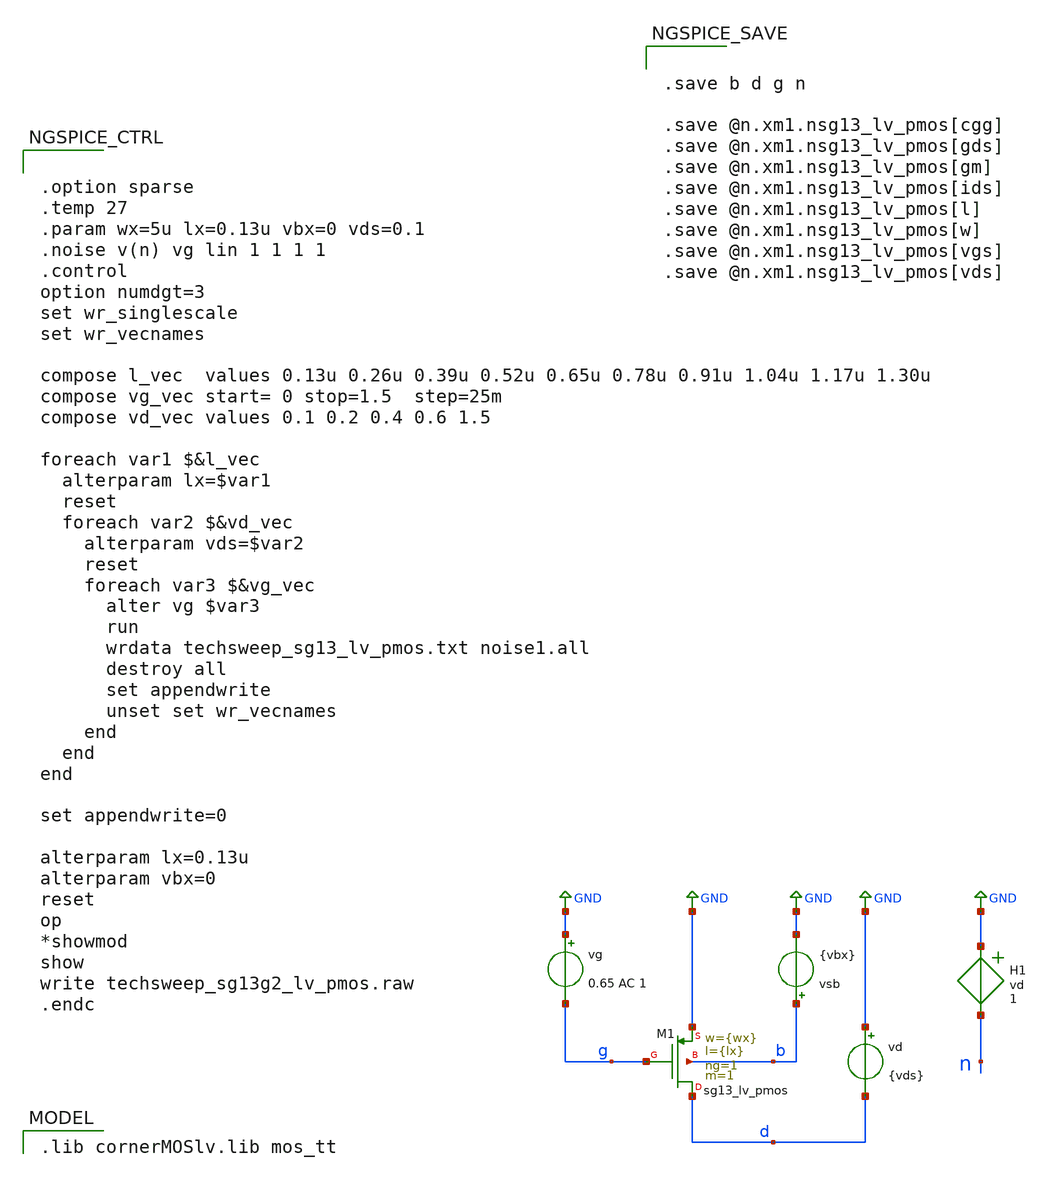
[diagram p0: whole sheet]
** sch_path: pmos.sch
**.subckt pmos
XM1 d g GND b sg13_lv_pmos w={wx} l={lx} ng=1 m=1 mm_ok=1
vd GND d {vds}
vsb b GND {vbx}
vg GND g 0.65 AC 1
H1 GND n vd 1
**** begin user architecture code
 .lib cornerMOSlv.lib mos_tt



.save b d g n

.save @n.xm1.nsg13_lv_pmos[cgg]
.save @n.xm1.nsg13_lv_pmos[gds]
.save @n.xm1.nsg13_lv_pmos[gm]
.save @n.xm1.nsg13_lv_pmos[ids]
.save @n.xm1.nsg13_lv_pmos[l]
.save @n.xm1.nsg13_lv_pmos[w]
.save @n.xm1.nsg13_lv_pmos[vgs]
.save @n.xm1.nsg13_lv_pmos[vds]





.option sparse
.temp 27
.param wx=5u lx=0.13u vbx=0 vds=0.1
.noise v(n) vg lin 1 1 1 1
.control
option numdgt=3
set wr_singlescale
set wr_vecnames

compose l_vec  values 0.13u 0.26u 0.39u 0.52u 0.65u 0.78u 0.91u 1.04u 1.17u 1.30u
compose vg_vec start= 0 stop=1.5  step=25m
compose vd_vec values 0.1 0.2 0.4 0.6 1.5

foreach var1 $&l_vec
  alterparam lx=$var1
  reset
  foreach var2 $&vd_vec
    alterparam vds=$var2
    reset
    foreach var3 $&vg_vec
      alter vg $var3
      run
      wrdata techsweep_sg13_lv_pmos.txt noise1.all
      destroy all
      set appendwrite
      unset set wr_vecnames
    end
  end
end

set appendwrite=0

alterparam lx=0.13u
alterparam vbx=0
reset
op
*showmod
show
write techsweep_sg13g2_lv_pmos.raw
.endc


**** end user architecture code
**.ends
.GLOBAL GND
.end
